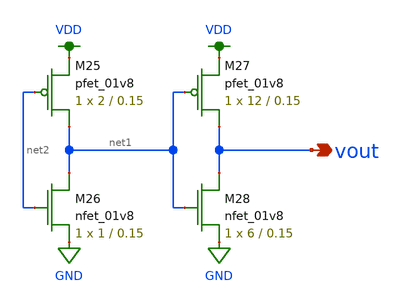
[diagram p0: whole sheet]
** sch_path: schematic/drive_buffer_lvs.sch
**.subckt drive_buffer_lvs vout
*.opin vout
XM25 net1 net2 VDD VDD sky130_fd_pr__pfet_01v8 L=0.15 W=2 nf=1 ad='int((nf+1)/2) * W/nf * 0.29' as='int((nf+2)/2) * W/nf * 0.29'
+ pd='2*int((nf+1)/2) * (W/nf + 0.29)' ps='2*int((nf+2)/2) * (W/nf + 0.29)' nrd='0.29 / W' nrs='0.29 / W'
+ sa=0 sb=0 sd=0 mult=1 m=1
XM26 net1 net2 GND GND sky130_fd_pr__nfet_01v8 L=0.15 W=1 nf=1 ad='int((nf+1)/2) * W/nf * 0.29' as='int((nf+2)/2) * W/nf * 0.29'
+ pd='2*int((nf+1)/2) * (W/nf + 0.29)' ps='2*int((nf+2)/2) * (W/nf + 0.29)' nrd='0.29 / W' nrs='0.29 / W'
+ sa=0 sb=0 sd=0 mult=1 m=1
XM27 vout net1 VDD VDD sky130_fd_pr__pfet_01v8 L=0.15 W=12 nf=1 ad='int((nf+1)/2) * W/nf * 0.29' as='int((nf+2)/2) * W/nf * 0.29'
+ pd='2*int((nf+1)/2) * (W/nf + 0.29)' ps='2*int((nf+2)/2) * (W/nf + 0.29)' nrd='0.29 / W' nrs='0.29 / W'
+ sa=0 sb=0 sd=0 mult=1 m=1
XM28 vout net1 GND GND sky130_fd_pr__nfet_01v8 L=0.15 W=6 nf=1 ad='int((nf+1)/2) * W/nf * 0.29' as='int((nf+2)/2) * W/nf * 0.29'
+ pd='2*int((nf+1)/2) * (W/nf + 0.29)' ps='2*int((nf+2)/2) * (W/nf + 0.29)' nrd='0.29 / W' nrs='0.29 / W'
+ sa=0 sb=0 sd=0 mult=1 m=1
**.ends
.GLOBAL VDD
.GLOBAL GND
.end
